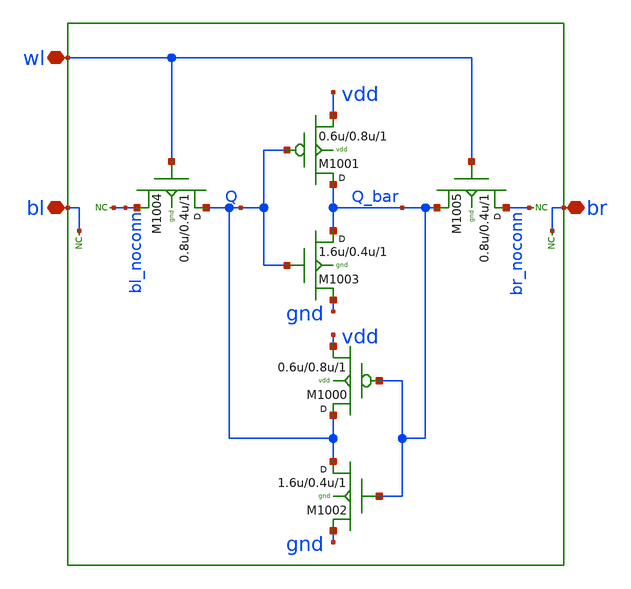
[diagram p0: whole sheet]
** sch_path: sram_4_16_scn4m/dummy_cell_1rw.sch
**.subckt dummy_cell_1rw bl br wl
*.iopin bl
*.iopin br
*.iopin wl
M1004 Q wl bl_noconn gnd n w=0.8u l=0.4u m=1
M1001 Q_bar Q vdd vdd p w=0.6u l=0.8u m=1
M1003 Q_bar Q gnd gnd n w=1.6u l=0.4u m=1
M1002 Q Q_bar gnd gnd n w=1.6u l=0.4u m=1
M1000 Q Q_bar vdd vdd p w=0.6u l=0.8u m=1
M1005 br_noconn wl Q_bar gnd n w=0.8u l=0.4u m=1
* noconn bl_noconn
* noconn br_noconn
* noconn br
* noconn bl
**.ends
.end
